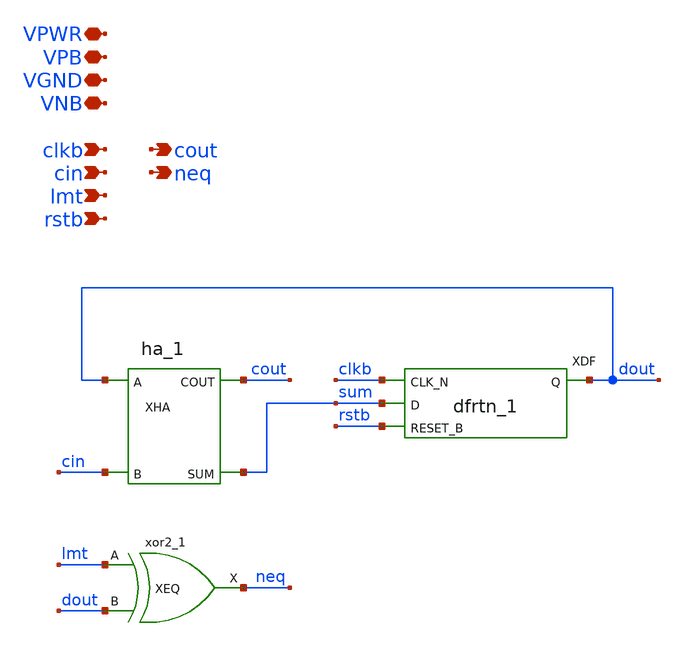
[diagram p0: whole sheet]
** sch_path: xschem/tiny_pll/tiny_pll_divider_cell.sch
**.subckt tiny_pll_divider_cell cin lmt clkb cout neq VPWR VPB VGND VNB rstb
*.ipin cin
*.ipin lmt
*.ipin clkb
*.opin cout
*.opin neq
*.iopin VPWR
*.iopin VPB
*.iopin VGND
*.iopin VNB
*.ipin rstb
XHA dout cin VGND VNB VPB VPWR cout sum sky130_fd_sc_hd__ha_1
XEQ lmt dout VGND VNB VPB VPWR neq sky130_fd_sc_hd__xor2_1
XDF clkb sum rstb VGND VNB VPB VPWR dout sky130_fd_sc_hd__dfrtn_1
**.ends
.end
